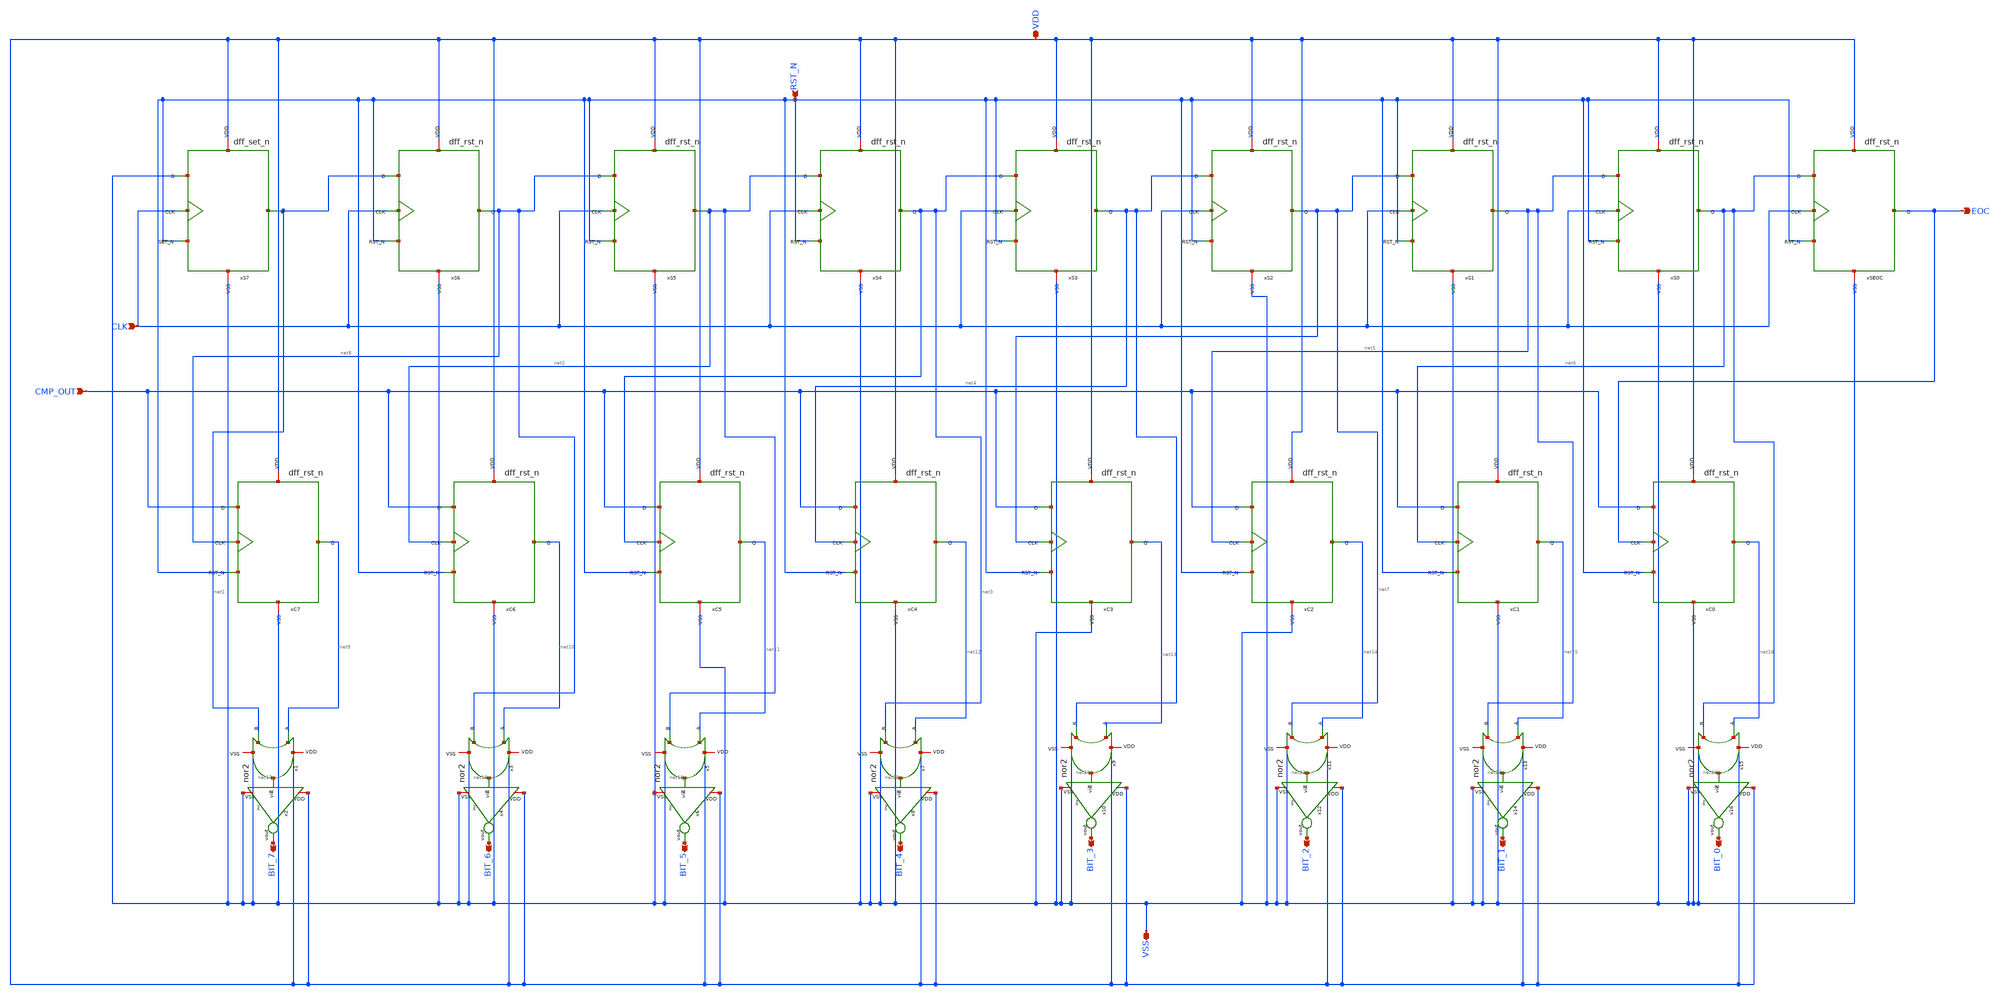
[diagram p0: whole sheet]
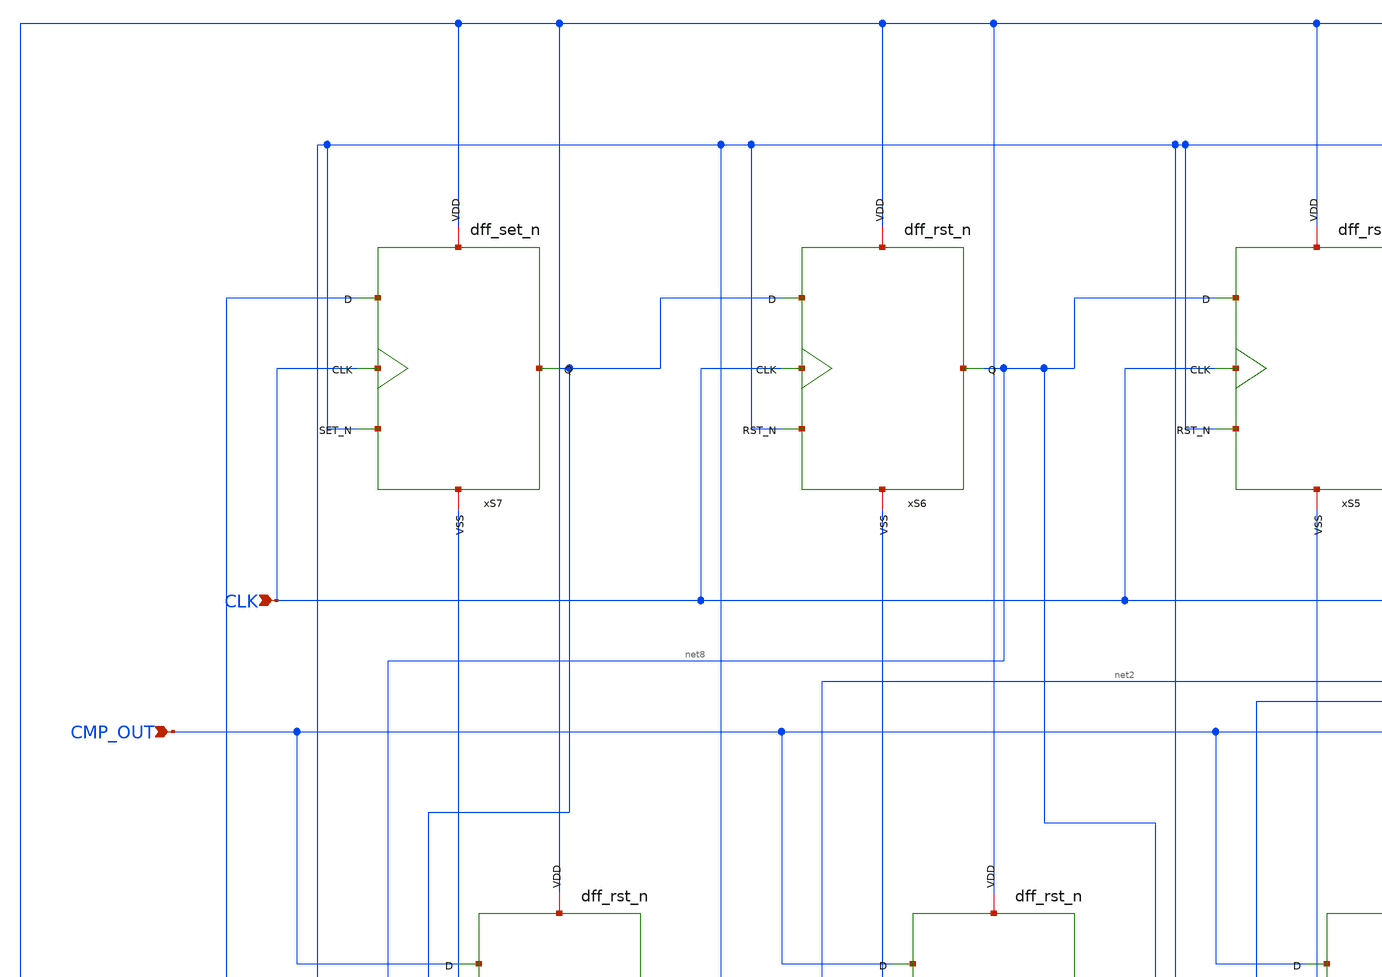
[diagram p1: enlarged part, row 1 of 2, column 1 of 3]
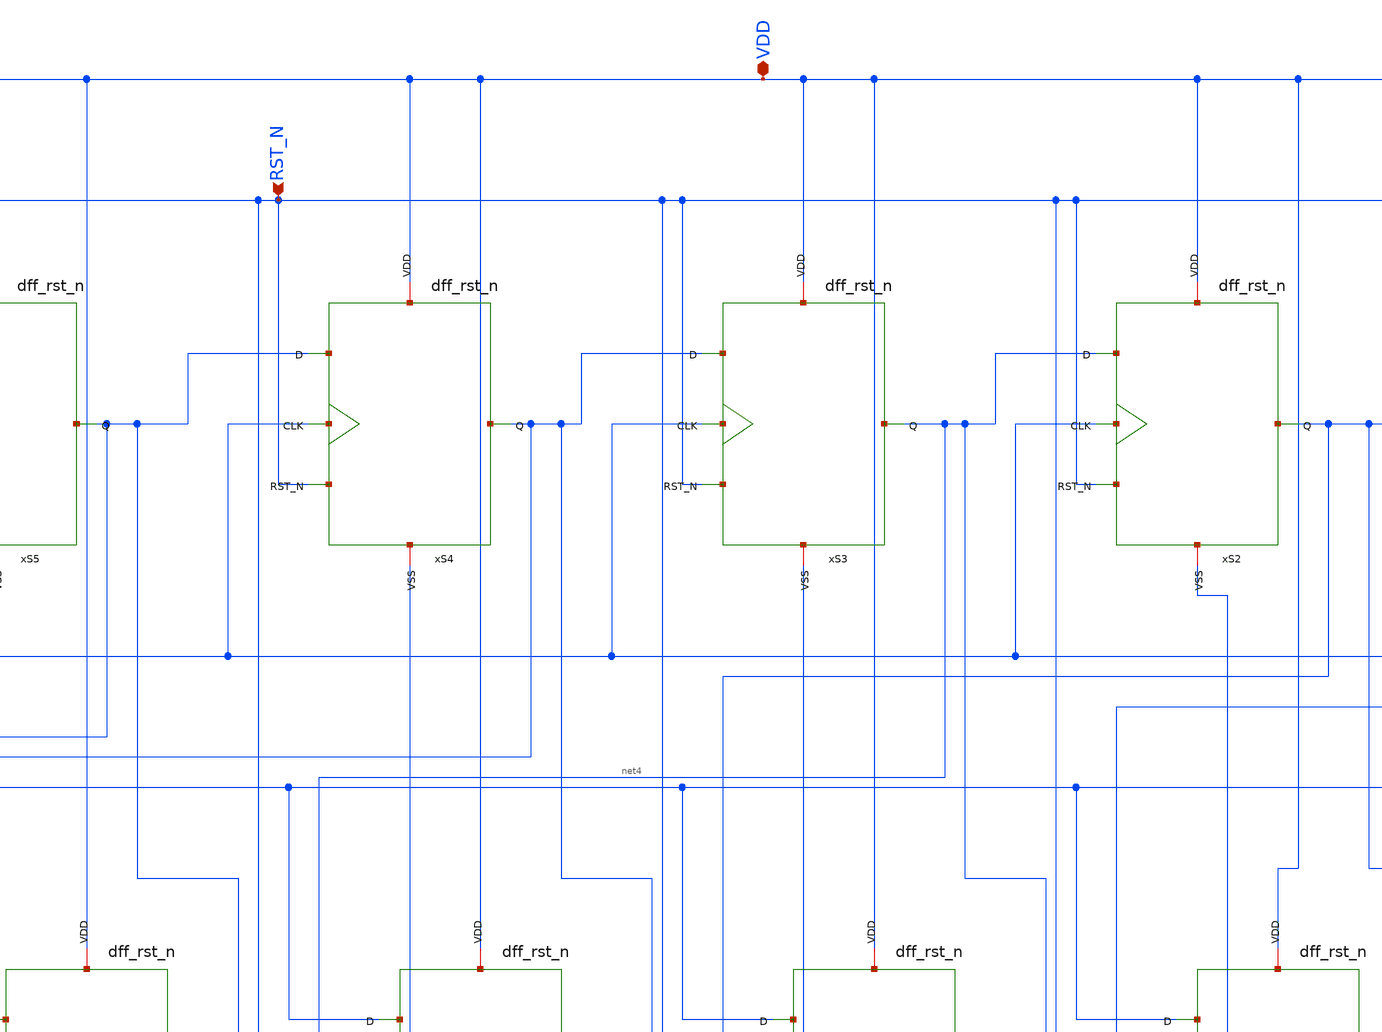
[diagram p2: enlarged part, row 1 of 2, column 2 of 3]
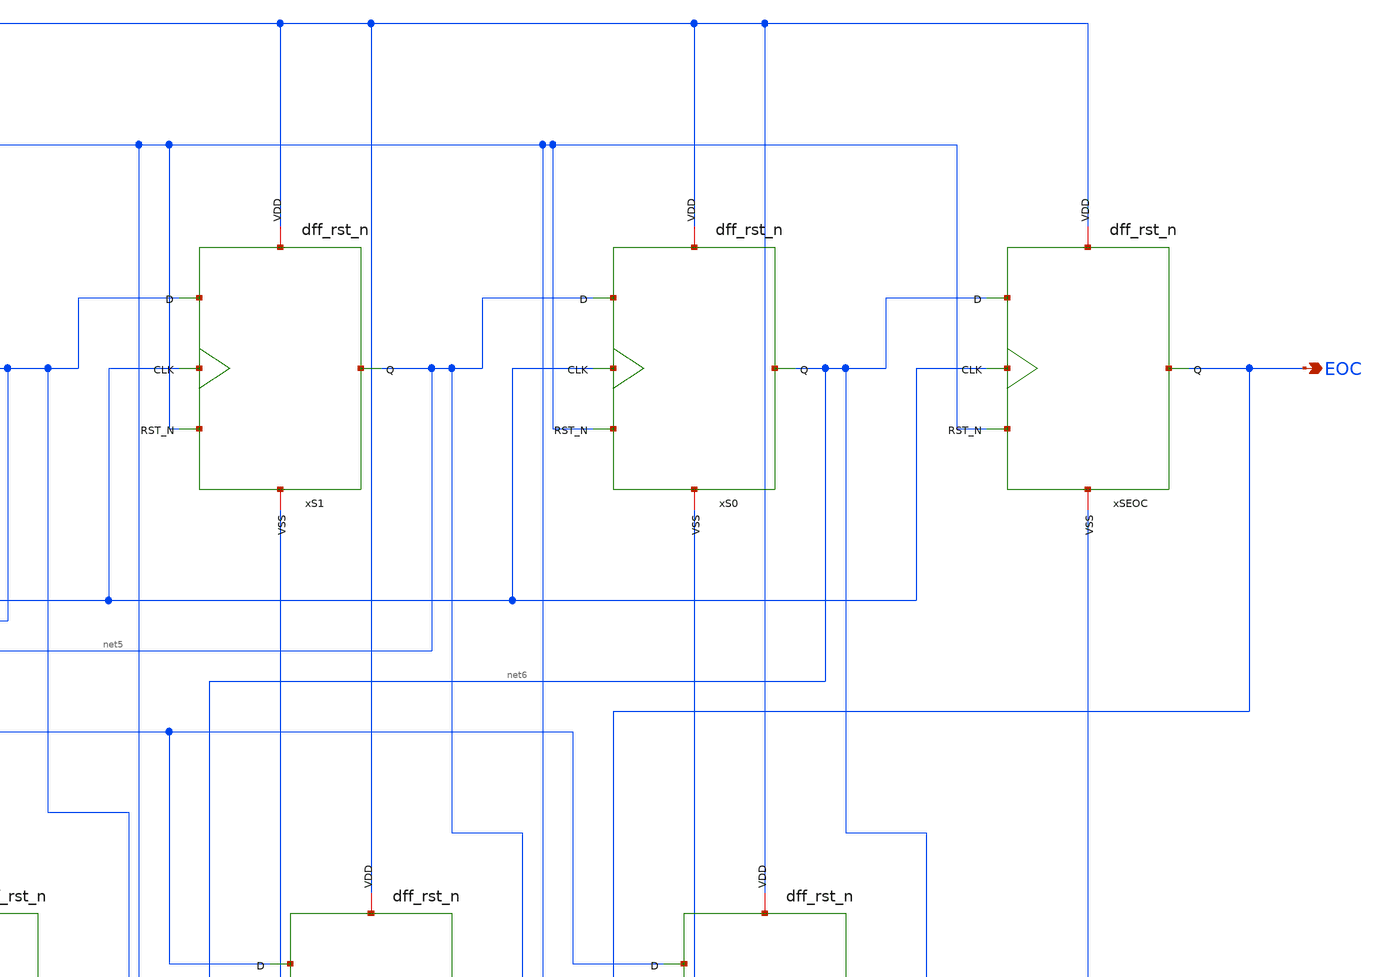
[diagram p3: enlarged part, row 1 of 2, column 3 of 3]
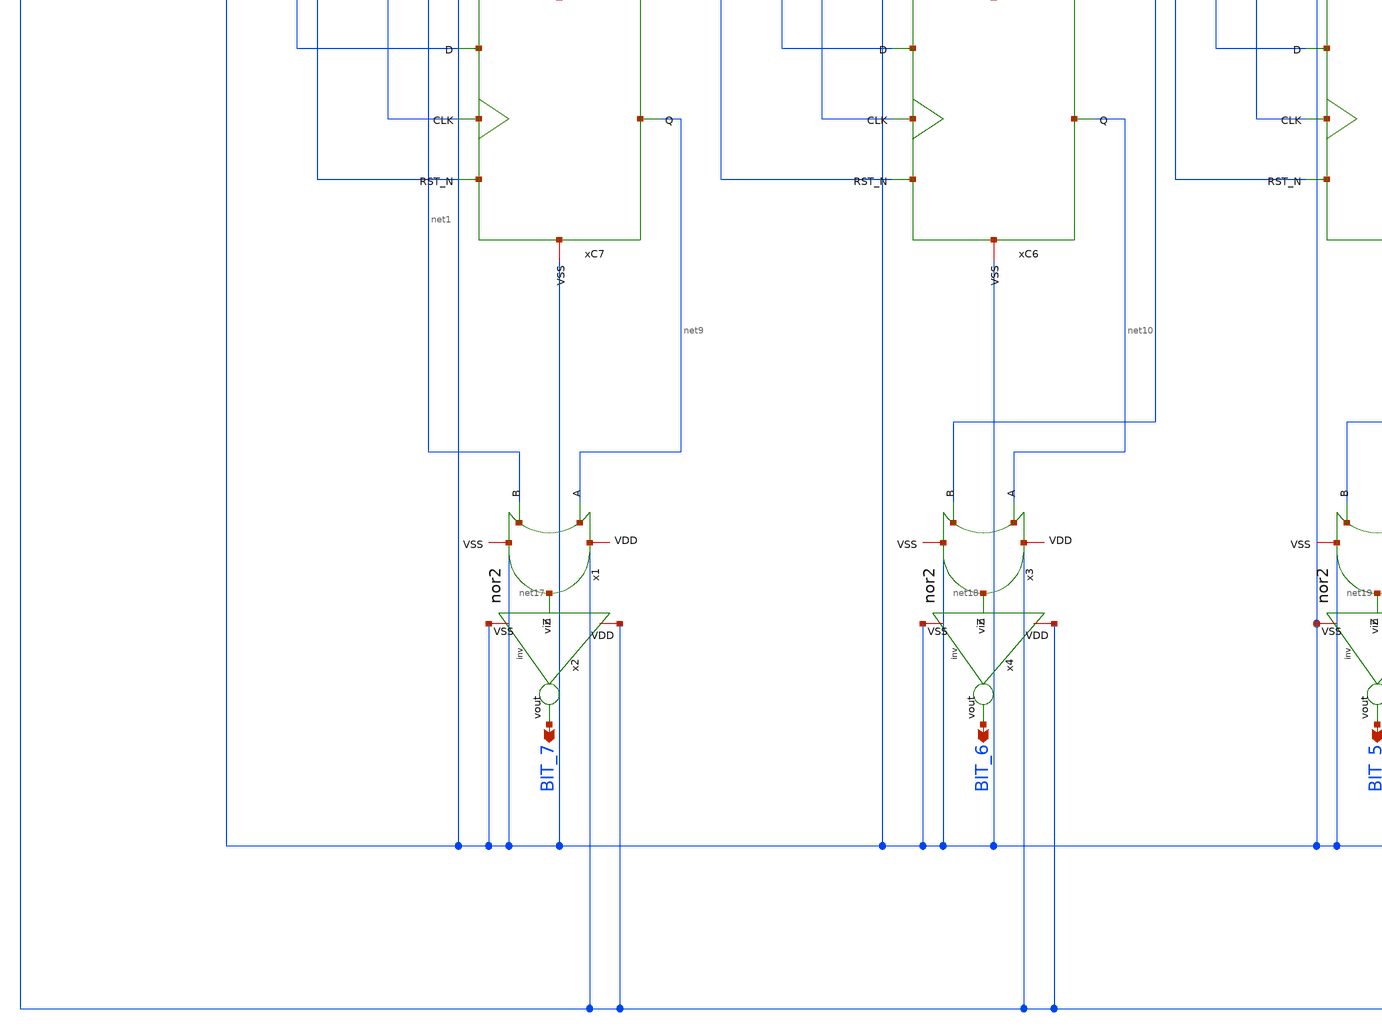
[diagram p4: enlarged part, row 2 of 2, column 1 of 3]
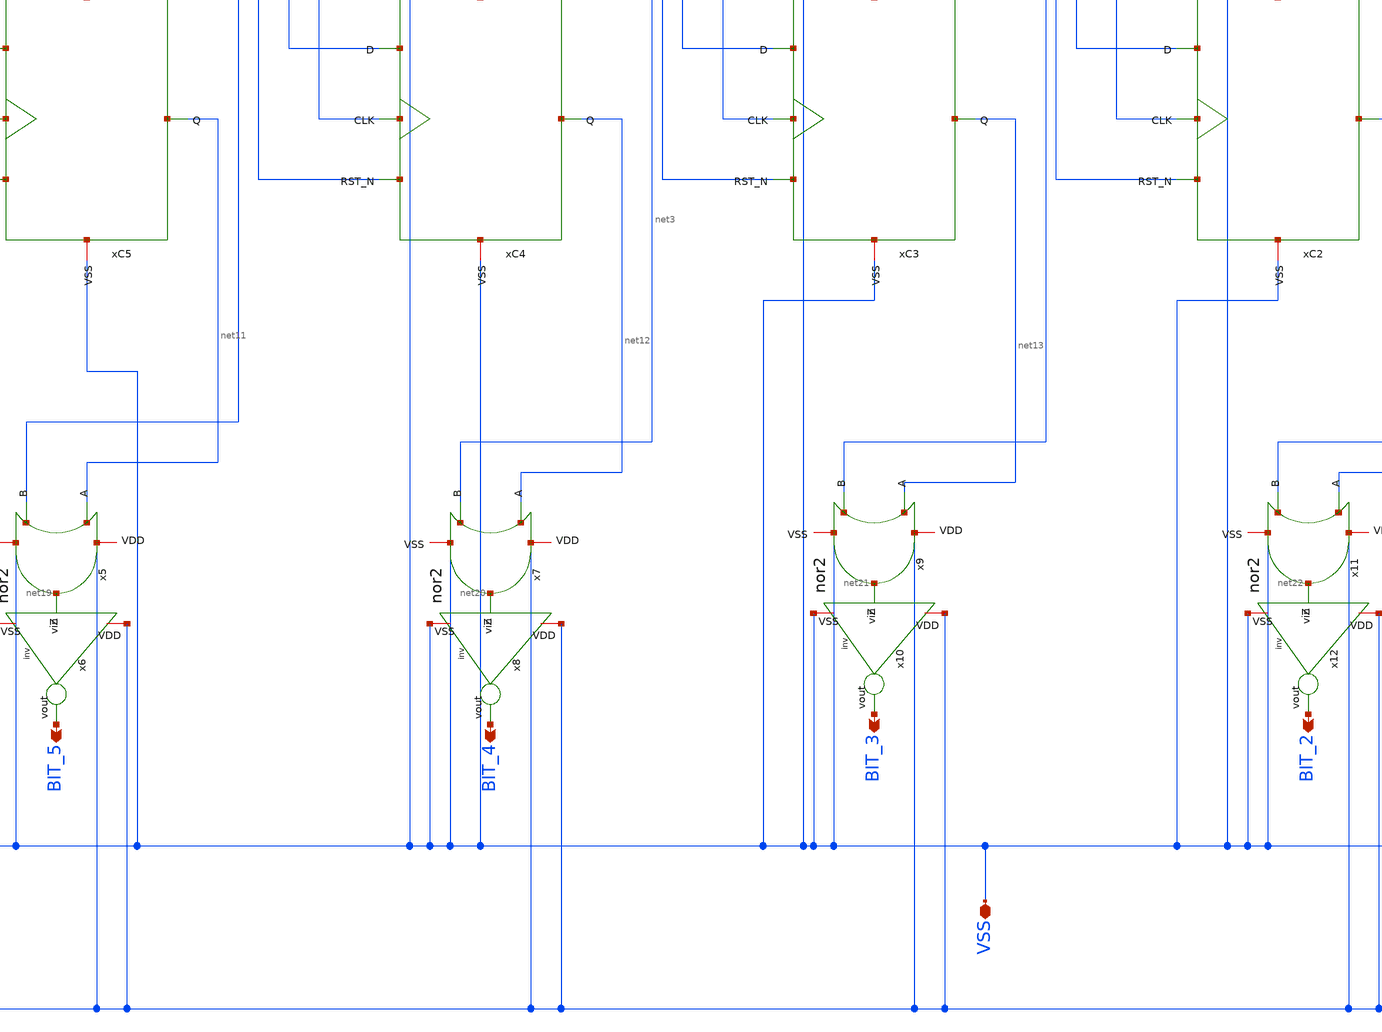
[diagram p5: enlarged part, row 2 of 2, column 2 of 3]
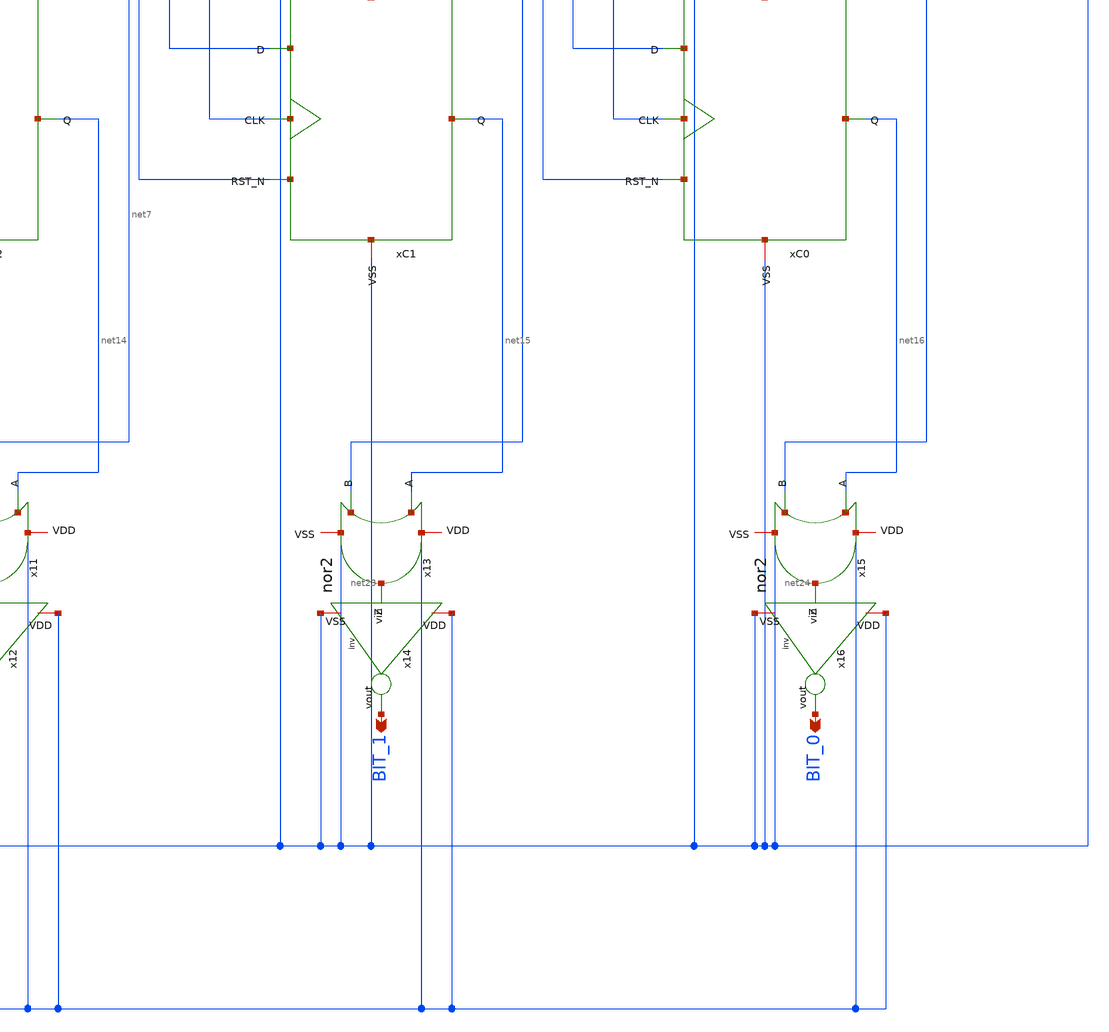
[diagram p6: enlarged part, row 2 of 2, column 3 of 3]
** sch_path: sar_logic/sar_designs/sar_logic/sar_logic.sch
**.subckt sar_logic VDD VSS BIT_7 BIT_6 BIT_5 BIT_4 BIT_3 BIT_2 BIT_1 BIT_0 EOC RST_N CMP_OUT CLK
*.iopin VDD
*.iopin VSS
*.opin BIT_7
*.opin BIT_6
*.opin BIT_5
*.opin BIT_4
*.opin BIT_3
*.opin BIT_2
*.opin BIT_1
*.opin BIT_0
*.opin EOC
*.ipin RST_N
*.ipin CMP_OUT
*.ipin CLK
xS7 VDD CLK VSS net1 RST_N VSS dff_set_n
xS6 VDD CLK net1 net8 RST_N VSS dff_rst_n
xS5 VDD CLK net8 net2 RST_N VSS dff_rst_n
xS4 VDD CLK net2 net3 RST_N VSS dff_rst_n
xS3 VDD CLK net3 net4 RST_N VSS dff_rst_n
xS2 VDD CLK net4 net7 RST_N VSS dff_rst_n
xS1 VDD CLK net7 net5 RST_N VSS dff_rst_n
xS0 VDD CLK net5 net6 RST_N VSS dff_rst_n
xSEOC VDD CLK net6 EOC RST_N VSS dff_rst_n
xC7 VDD net8 CMP_OUT net9 RST_N VSS dff_rst_n
xC6 VDD net2 CMP_OUT net10 RST_N VSS dff_rst_n
xC5 VDD net3 CMP_OUT net11 RST_N VSS dff_rst_n
xC4 VDD net4 CMP_OUT net12 RST_N VSS dff_rst_n
xC3 VDD net7 CMP_OUT net13 RST_N VSS dff_rst_n
xC2 VDD net5 CMP_OUT net14 RST_N VSS dff_rst_n
xC1 VDD net6 CMP_OUT net15 RST_N VSS dff_rst_n
xC0 VDD EOC CMP_OUT net16 RST_N VSS dff_rst_n
x1 VDD net9 net1 net17 VSS nor2
x2 VDD net17 BIT_7 VSS inv
x3 VDD net10 net8 net18 VSS nor2
x4 VDD net18 BIT_6 VSS inv
x5 VDD net11 net2 net19 VSS nor2
x6 VDD net19 BIT_5 VSS inv
x7 VDD net12 net3 net20 VSS nor2
x8 VDD net20 BIT_4 VSS inv
x9 VDD net13 net4 net21 VSS nor2
x10 VDD net21 BIT_3 VSS inv
x11 VDD net14 net7 net22 VSS nor2
x12 VDD net22 BIT_2 VSS inv
x13 VDD net15 net5 net23 VSS nor2
x14 VDD net23 BIT_1 VSS inv
x15 VDD net16 net6 net24 VSS nor2
x16 VDD net24 BIT_0 VSS inv
**.ends
.end
